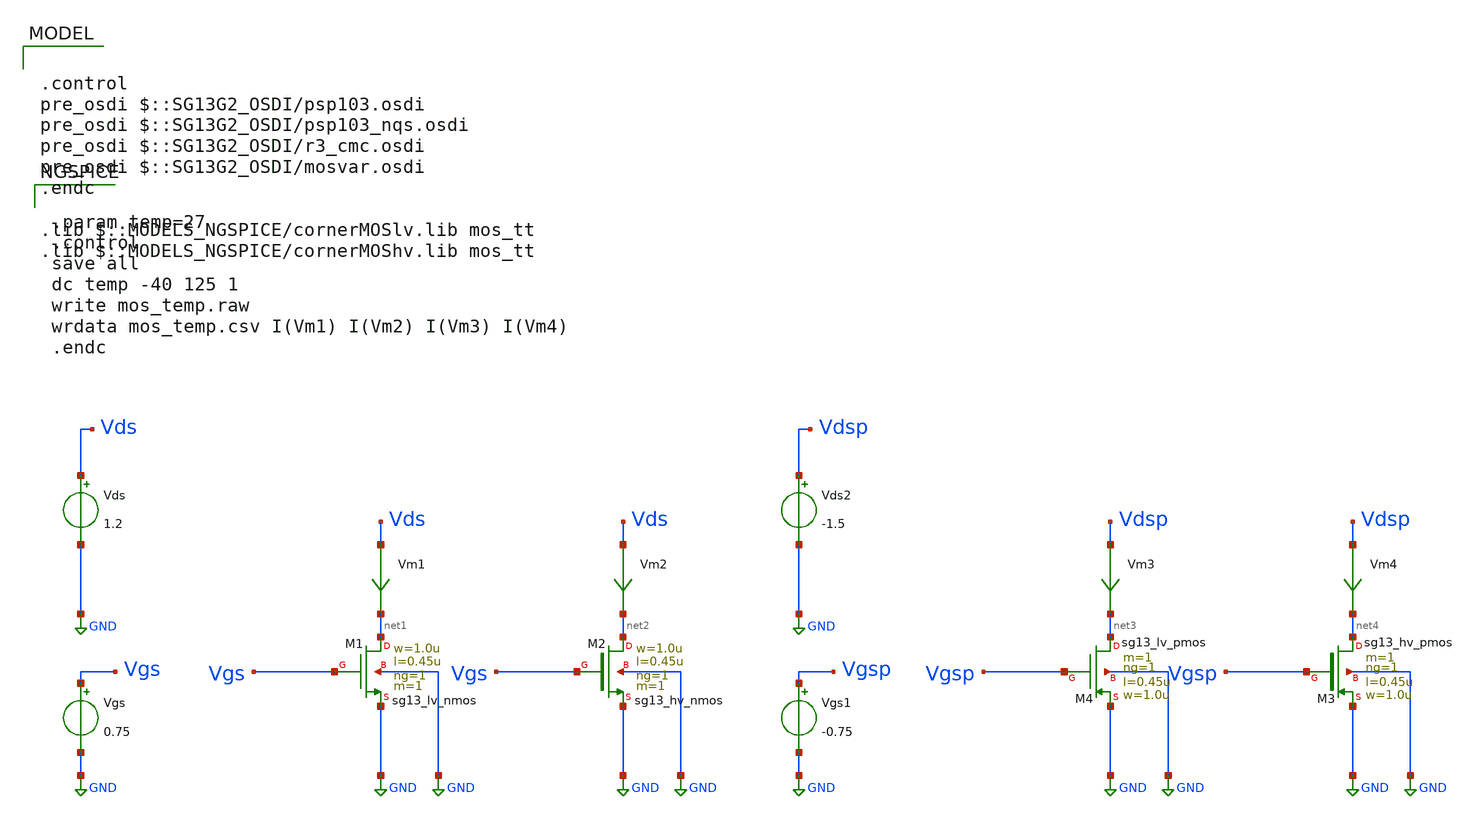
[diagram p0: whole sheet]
** sch_path: ihp-sg13g2/xschem_libs/sg13g2_tests/dc_mos_temp/schematic/dc_mos_temp.sch
* Copyright 2023 IHP PDK Authors
**.subckt dc_mos_temp
Vgs Vgs GND 0.75
Vds Vds GND 1.2
Vm1 Vds net1 0
.save i(vm1)
Vm2 Vds net2 0
.save i(vm2)
Vm3 Vdsp net3 0
.save i(vm3)
Vm4 Vdsp net4 0
.save i(vm4)
Vgs1 Vgsp GND -0.75
Vds2 Vdsp GND -1.5
XM1 net1 Vgs GND GND sg13_lv_nmos w=1.0u l=0.45u ng=1 m=1 mm_ok=1
XM2 net2 Vgs GND GND sg13_hv_nmos w=1.0u l=0.45u ng=1 m=1 mm_ok=1
XM3 net4 Vgsp GND GND sg13_hv_pmos w=1.0u l=0.45u ng=1 m=1 mm_ok=1
XM4 net3 Vgsp GND GND sg13_lv_pmos w=1.0u l=0.45u ng=1 m=1 mm_ok=1
**** begin user architecture code

.control
pre_osdi $::SG13G2_OSDI/psp103.osdi
pre_osdi $::SG13G2_OSDI/psp103_nqs.osdi
pre_osdi $::SG13G2_OSDI/r3_cmc.osdi
pre_osdi $::SG13G2_OSDI/mosvar.osdi
.endc

.lib $::MODELS_NGSPICE/cornerMOSlv.lib mos_tt
.lib $::MODELS_NGSPICE/cornerMOShv.lib mos_tt



.param temp=27
.control
save all
dc temp -40 125 1
write mos_temp.raw
wrdata mos_temp.csv I(Vm1) I(Vm2) I(Vm3) I(Vm4)
.endc


**** end user architecture code
**.ends
.GLOBAL GND
.end
